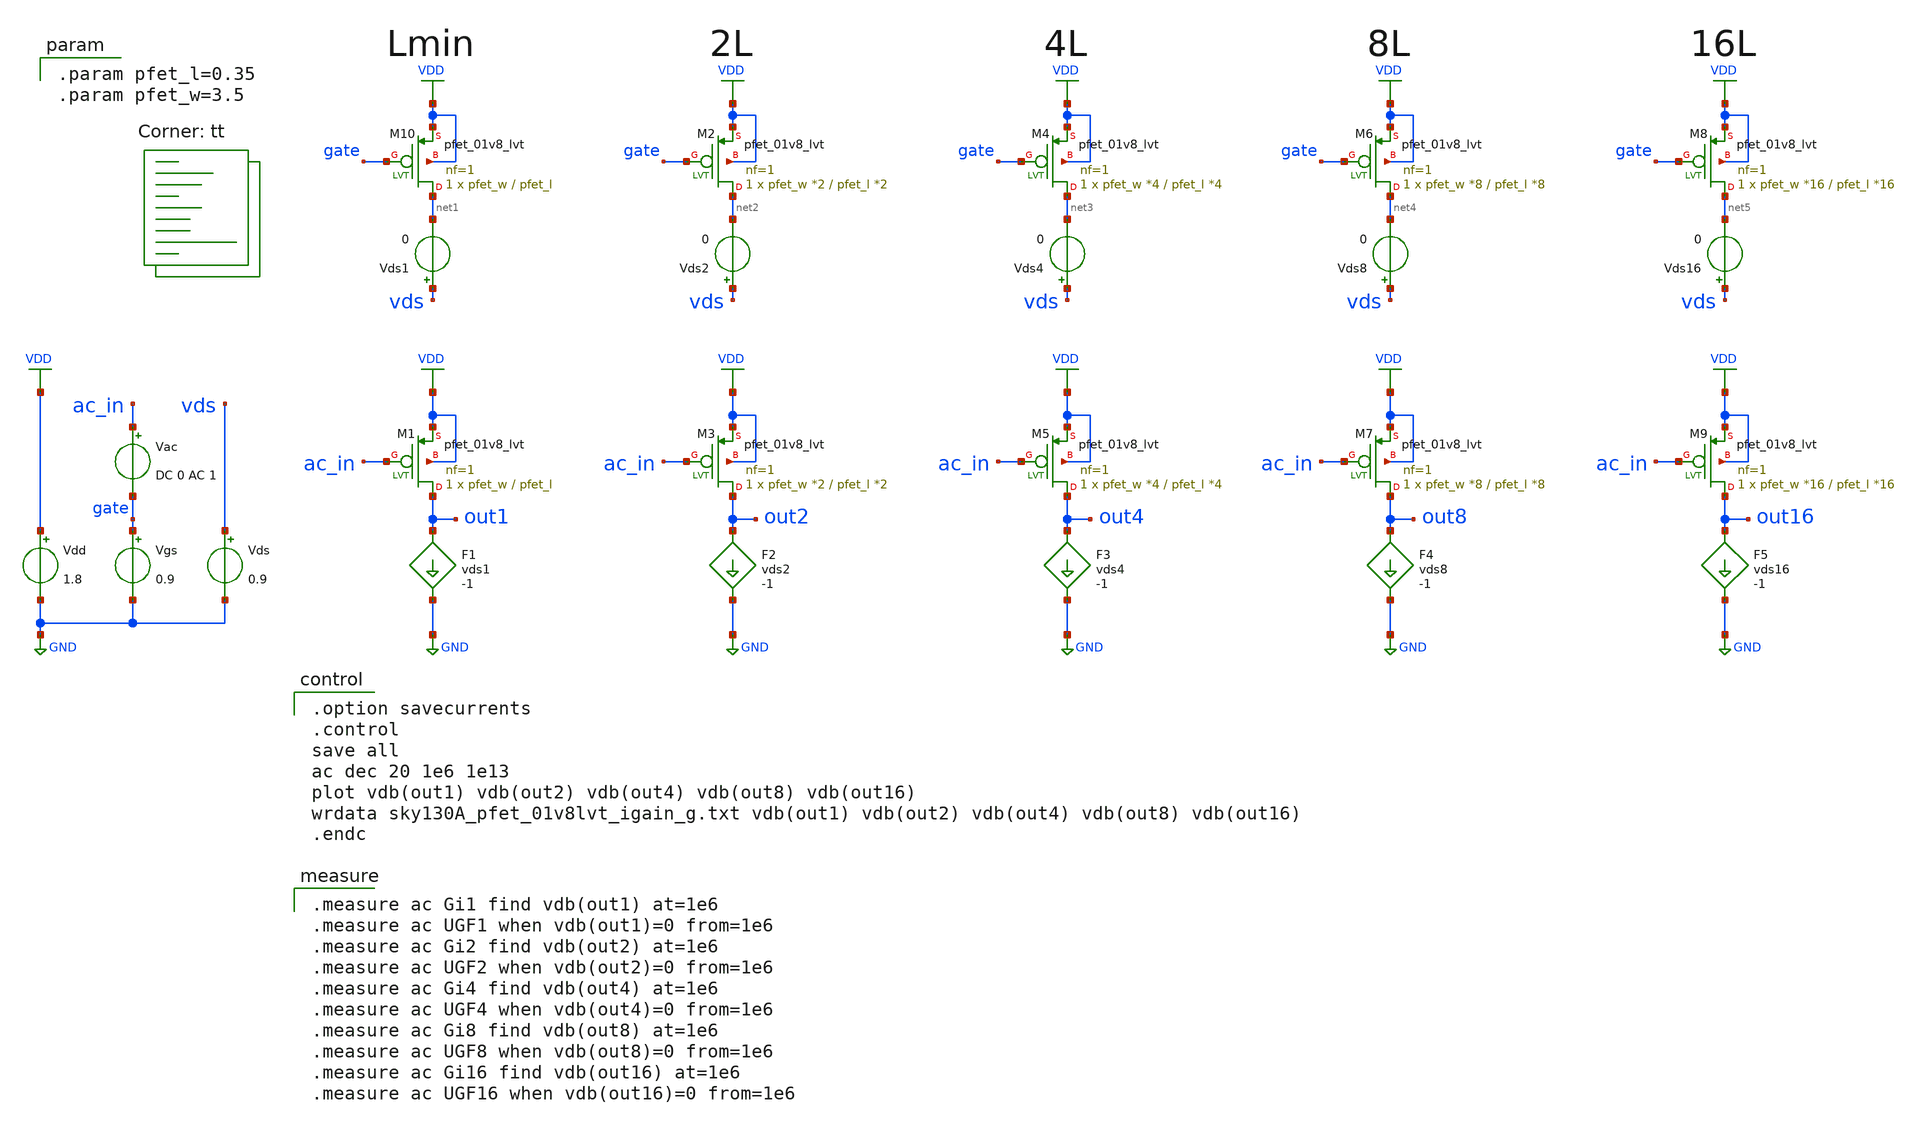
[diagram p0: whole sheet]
** sch_path: xschem/MOSFET/sky130A_pfet_01v8lvt_igain.sch
**.subckt sky130A_pfet_01v8lvt_igain
Vgs gate GND 0.9
Vdd VDD GND 1.8
F1 out1 GND vds1 -1
Vds vds GND 0.9
Vac ac_in gate DC 0 AC 1
Vds1 vds net1 0
F2 out2 GND vds2 -1
Vds2 vds net2 0
F3 out4 GND vds4 -1
Vds4 vds net3 0
F4 out8 GND vds8 -1
Vds8 vds net4 0
F5 out16 GND vds16 -1
Vds16 vds net5 0
XM10 net1 gate VDD VDD sky130_fd_pr__pfet_01v8_lvt L=pfet_l W=pfet_w nf=1 ad='int((1 + 1)/2) * pfet_w / 1 * 0.29'
+ as='int((1 + 2)/2) * pfet_w / 1 * 0.29' pd='2*int((1 + 1)/2) * (pfet_w / 1 + 0.29)' ps='2*int((1 + 2)/2) * (pfet_w / 1 + 0.29)'
+ nrd='0.29 / pfet_w ' nrs='0.29 / pfet_w ' sa=0 sb=0 sd=0 mult=1 m=1
XM1 out1 ac_in VDD VDD sky130_fd_pr__pfet_01v8_lvt L=pfet_l W=pfet_w nf=1 ad='int((1 + 1)/2) * pfet_w / 1 * 0.29'
+ as='int((1 + 2)/2) * pfet_w / 1 * 0.29' pd='2*int((1 + 1)/2) * (pfet_w / 1 + 0.29)' ps='2*int((1 + 2)/2) * (pfet_w / 1 + 0.29)'
+ nrd='0.29 / pfet_w ' nrs='0.29 / pfet_w ' sa=0 sb=0 sd=0 mult=1 m=1
XM2 net2 gate VDD VDD sky130_fd_pr__pfet_01v8_lvt L=pfet_l *2 W=pfet_w *2 nf=1 ad='int((1 + 1)/2) * pfet_w *2 / 1 * 0.29'
+ as='int((1 + 2)/2) * pfet_w *2 / 1 * 0.29' pd='2*int((1 + 1)/2) * (pfet_w *2 / 1 + 0.29)' ps='2*int((1 + 2)/2) * (pfet_w *2 / 1 + 0.29)'
+ nrd='0.29 / pfet_w *2 ' nrs='0.29 / pfet_w *2 ' sa=0 sb=0 sd=0 mult=1 m=1
XM3 out2 ac_in VDD VDD sky130_fd_pr__pfet_01v8_lvt L=pfet_l *2 W=pfet_w *2 nf=1 ad='int((1 + 1)/2) * pfet_w *2 / 1 * 0.29'
+ as='int((1 + 2)/2) * pfet_w *2 / 1 * 0.29' pd='2*int((1 + 1)/2) * (pfet_w *2 / 1 + 0.29)' ps='2*int((1 + 2)/2) * (pfet_w *2 / 1 + 0.29)'
+ nrd='0.29 / pfet_w *2 ' nrs='0.29 / pfet_w *2 ' sa=0 sb=0 sd=0 mult=1 m=1
XM4 net3 gate VDD VDD sky130_fd_pr__pfet_01v8_lvt L=pfet_l *4 W=pfet_w *4 nf=1 ad='int((1 + 1)/2) * pfet_w *4 / 1 * 0.29'
+ as='int((1 + 2)/2) * pfet_w *4 / 1 * 0.29' pd='2*int((1 + 1)/2) * (pfet_w *4 / 1 + 0.29)' ps='2*int((1 + 2)/2) * (pfet_w *4 / 1 + 0.29)'
+ nrd='0.29 / pfet_w *4 ' nrs='0.29 / pfet_w *4 ' sa=0 sb=0 sd=0 mult=1 m=1
XM5 out4 ac_in VDD VDD sky130_fd_pr__pfet_01v8_lvt L=pfet_l *4 W=pfet_w *4 nf=1 ad='int((1 + 1)/2) * pfet_w *4 / 1 * 0.29'
+ as='int((1 + 2)/2) * pfet_w *4 / 1 * 0.29' pd='2*int((1 + 1)/2) * (pfet_w *4 / 1 + 0.29)' ps='2*int((1 + 2)/2) * (pfet_w *4 / 1 + 0.29)'
+ nrd='0.29 / pfet_w *4 ' nrs='0.29 / pfet_w *4 ' sa=0 sb=0 sd=0 mult=1 m=1
XM6 net4 gate VDD VDD sky130_fd_pr__pfet_01v8_lvt L=pfet_l *8 W=pfet_w *8 nf=1 ad='int((1 + 1)/2) * pfet_w *8 / 1 * 0.29'
+ as='int((1 + 2)/2) * pfet_w *8 / 1 * 0.29' pd='2*int((1 + 1)/2) * (pfet_w *8 / 1 + 0.29)' ps='2*int((1 + 2)/2) * (pfet_w *8 / 1 + 0.29)'
+ nrd='0.29 / pfet_w *8 ' nrs='0.29 / pfet_w *8 ' sa=0 sb=0 sd=0 mult=1 m=1
XM7 out8 ac_in VDD VDD sky130_fd_pr__pfet_01v8_lvt L=pfet_l *8 W=pfet_w *8 nf=1 ad='int((1 + 1)/2) * pfet_w *8 / 1 * 0.29'
+ as='int((1 + 2)/2) * pfet_w *8 / 1 * 0.29' pd='2*int((1 + 1)/2) * (pfet_w *8 / 1 + 0.29)' ps='2*int((1 + 2)/2) * (pfet_w *8 / 1 + 0.29)'
+ nrd='0.29 / pfet_w *8 ' nrs='0.29 / pfet_w *8 ' sa=0 sb=0 sd=0 mult=1 m=1
XM8 net5 gate VDD VDD sky130_fd_pr__pfet_01v8_lvt L=pfet_l *16 W=pfet_w *16 nf=1 ad='int((1 + 1)/2) * pfet_w *16 / 1 * 0.29'
+ as='int((1 + 2)/2) * pfet_w *16 / 1 * 0.29' pd='2*int((1 + 1)/2) * (pfet_w *16 / 1 + 0.29)' ps='2*int((1 + 2)/2) * (pfet_w *16 / 1 + 0.29)'
+ nrd='0.29 / pfet_w *16 ' nrs='0.29 / pfet_w *16 ' sa=0 sb=0 sd=0 mult=1 m=1
XM9 out16 ac_in VDD VDD sky130_fd_pr__pfet_01v8_lvt L=pfet_l *16 W=pfet_w *16 nf=1 ad='int((1 + 1)/2) * pfet_w *16 / 1 * 0.29'
+ as='int((1 + 2)/2) * pfet_w *16 / 1 * 0.29' pd='2*int((1 + 1)/2) * (pfet_w *16 / 1 + 0.29)' ps='2*int((1 + 2)/2) * (pfet_w *16 / 1 + 0.29)'
+ nrd='0.29 / pfet_w *16 ' nrs='0.29 / pfet_w *16 ' sa=0 sb=0 sd=0 mult=1 m=1
**** begin user architecture code

.option savecurrents
.control
save all
ac dec 20 1e6 1e13
plot vdb(out1) vdb(out2) vdb(out4) vdb(out8) vdb(out16)
wrdata sky130A_pfet_01v8lvt_igain_g.txt vdb(out1) vdb(out2) vdb(out4) vdb(out8) vdb(out16)
.endc


.param pfet_l=0.35
.param pfet_w=3.5


.measure ac Gi1 find vdb(out1) at=1e6
.measure ac UGF1 when vdb(out1)=0 from=1e6
.measure ac Gi2 find vdb(out2) at=1e6
.measure ac UGF2 when vdb(out2)=0 from=1e6
.measure ac Gi4 find vdb(out4) at=1e6
.measure ac UGF4 when vdb(out4)=0 from=1e6
.measure ac Gi8 find vdb(out8) at=1e6
.measure ac UGF8 when vdb(out8)=0 from=1e6
.measure ac Gi16 find vdb(out16) at=1e6
.measure ac UGF16 when vdb(out16)=0 from=1e6

.lib $::SKYWATER_MODELS/sky130.lib.spice tt
**** end user architecture code
**.ends
.GLOBAL GND
.GLOBAL VDD
.end
